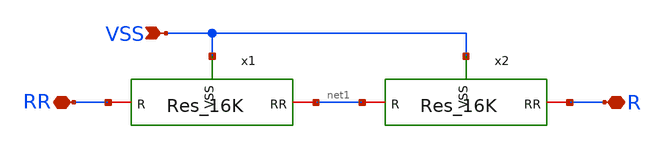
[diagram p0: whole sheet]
** sch_path: Res_32K.sch
**.subckt Res_32K R RR VSS
*.iopin R
*.iopin RR
*.ipin VSS
x1 VSS net1 RR Res_16K
x2 VSS R net1 Res_16K
**.ends

* expanding   symbol:  ../xschem/Res_16K.sym # of pins=3
** sym_path: Res_16K.sym
** sch_path: Res_16K.sch
.subckt Res_16K VSS RR R
*.iopin R
*.iopin RR
*.ipin VSS
x1 VSS net1 RR Res_8K
x2 VSS R net1 Res_8K
.ends


* expanding   symbol:  ../xschem/Res_8K.sym # of pins=3
** sym_path: Res_8K.sym
** sch_path: Res_8K.sch
.subckt Res_8K VSS RR R
*.iopin R
*.iopin RR
*.ipin VSS
x1 VSS net1 RR Res_4K
x2 VSS R net1 Res_4K
.ends


* expanding   symbol:  ../xschem/Res_4K.sym # of pins=3
** sym_path: Res_4K.sym
** sch_path: Res_4K.sch
.subckt Res_4K VSS RR R
*.iopin R
*.iopin RR
*.ipin VSS
x1 VSS net1 RR Res_2K
x2 VSS R net1 Res_2K
.ends


* expanding   symbol:  ../xschem/Res_2K.sym # of pins=3
** sym_path: Res_2K.sym
** sch_path: Res_2K.sch
.subckt Res_2K VSS RR R
*.iopin R
*.iopin RR
*.ipin VSS
XR2 RR net1 VSS sky130_fd_pr__res_high_po_0p69 L=19.55 mult=10 m=10
XR1 net1 R VSS sky130_fd_pr__res_high_po_0p69 L=19.55 mult=10 m=10
.ends

.end
